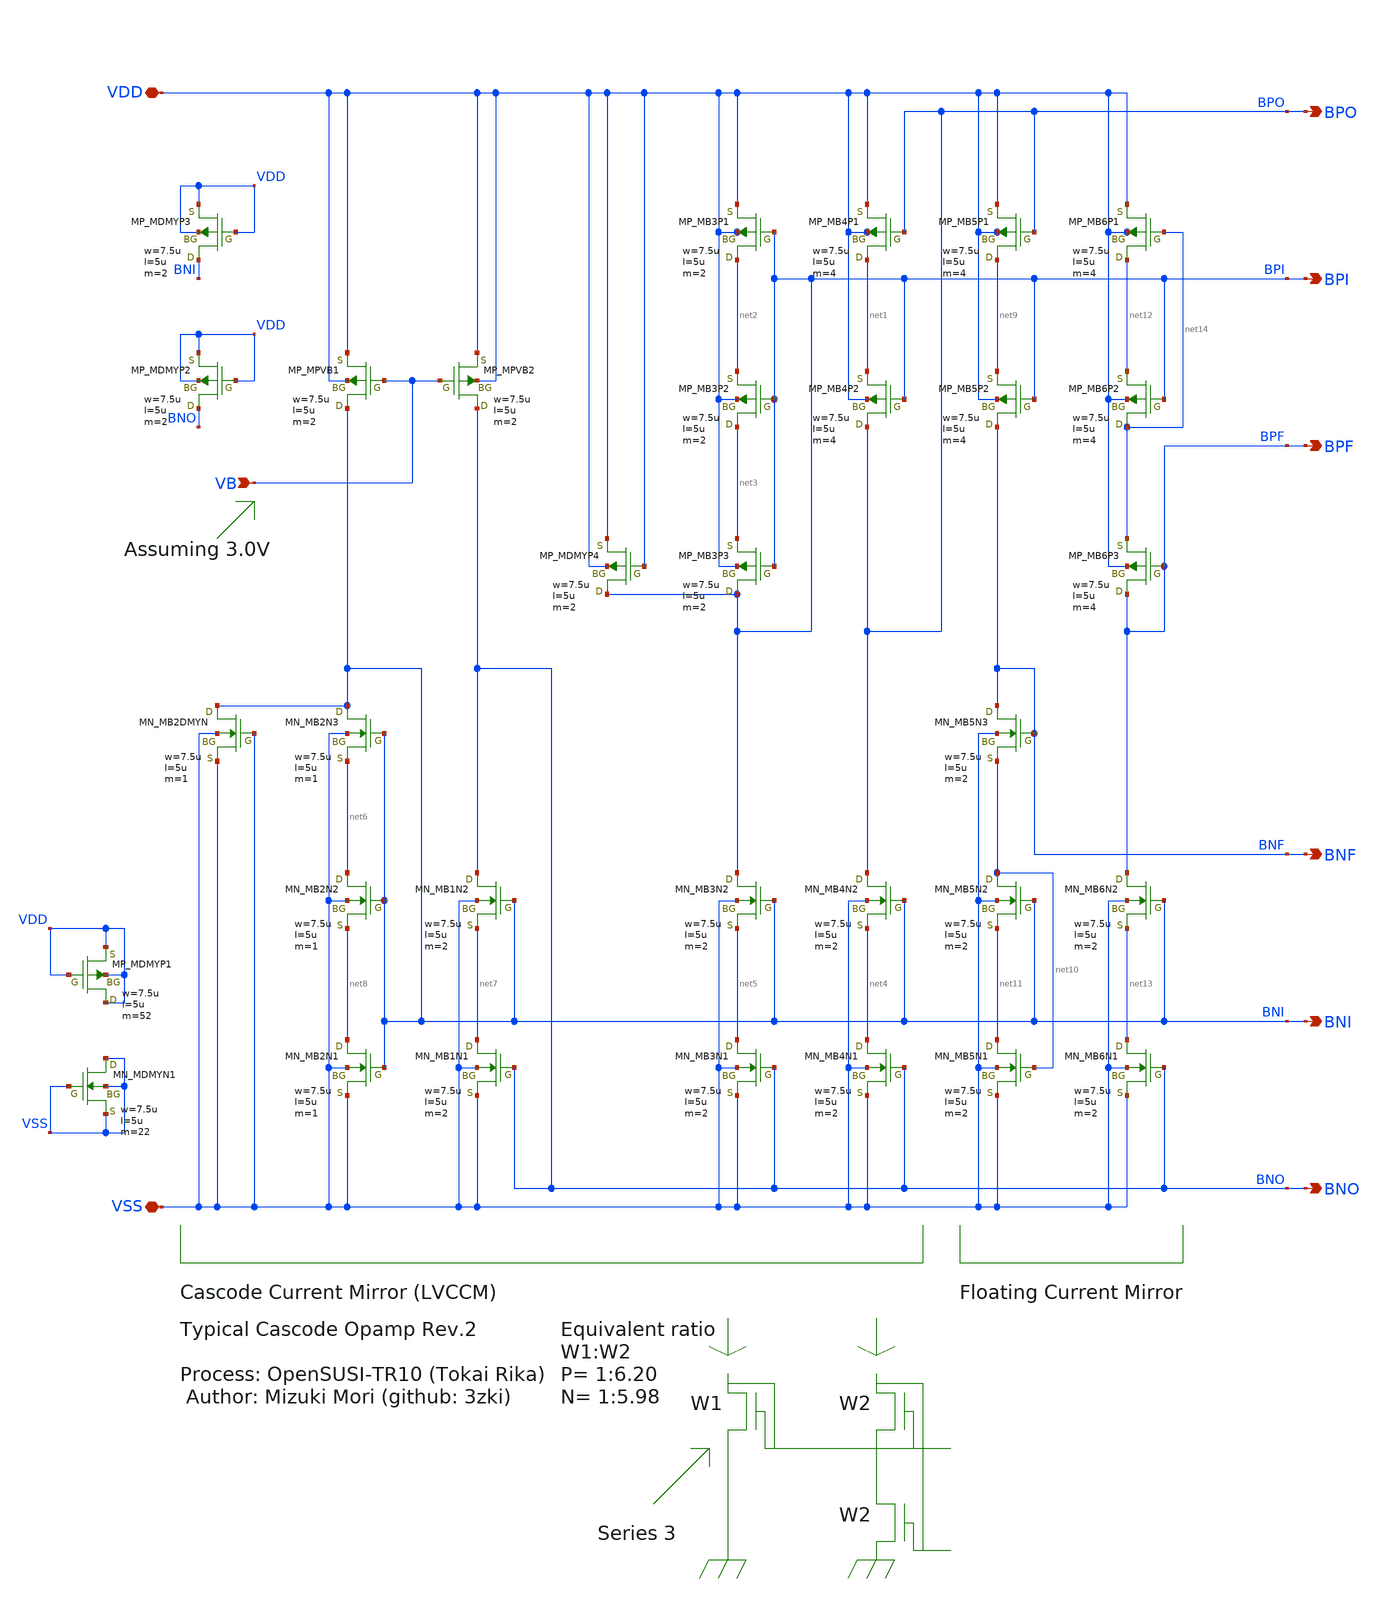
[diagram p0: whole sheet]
** sch_path: OpenSUSI-TR10/opamp_r2r_audio/opamp_r2r_CS.sch
**.subckt opamp_r2r_CS VDD VSS VB BPO BPI BPF BNF BNI BNO
*.iopin VDD
*.iopin VSS
*.ipin VB
*.opin BPO
*.opin BPI
*.opin BPF
*.opin BNF
*.opin BNI
*.opin BNO
XMB4P1 net1 BPO VDD VDD PMOS w=7.5u l=5u as=0 ad=0 ps=0 pd=0 nrd=0 nrs=0 m=4
XMB4P2 BPO BPI net1 VDD PMOS w=7.5u l=5u as=0 ad=0 ps=0 pd=0 nrd=0 nrs=0 m=4
XMB3P1 net2 BPI VDD VDD PMOS w=7.5u l=5u as=0 ad=0 ps=0 pd=0 nrd=0 nrs=0 m=2
XMB3P2 net3 BPI net2 VDD PMOS w=7.5u l=5u as=0 ad=0 ps=0 pd=0 nrd=0 nrs=0 m=2
XMB3P3 BPI BPI net3 VDD PMOS w=7.5u l=5u as=0 ad=0 ps=0 pd=0 nrd=0 nrs=0 m=2
XMB4N2 BPO BNI net4 VSS NMOS w=7.5u l=5u as=0 ad=0 ps=0 pd=0 nrd=0 nrs=0 m=2
XMB3N2 BPI BNI net5 VSS NMOS w=7.5u l=5u as=0 ad=0 ps=0 pd=0 nrd=0 nrs=0 m=2
XMB4N1 net4 BNO VSS VSS NMOS w=7.5u l=5u as=0 ad=0 ps=0 pd=0 nrd=0 nrs=0 m=2
XMB3N1 net5 BNO VSS VSS NMOS w=7.5u l=5u as=0 ad=0 ps=0 pd=0 nrd=0 nrs=0 m=2
XMB1N2 BNO BNI net7 VSS NMOS w=7.5u l=5u as=0 ad=0 ps=0 pd=0 nrd=0 nrs=0 m=2
XMB2N2 net6 BNI net8 VSS NMOS w=7.5u l=5u as=0 ad=0 ps=0 pd=0 nrd=0 nrs=0 m=1
XMB1N1 net7 BNO VSS VSS NMOS w=7.5u l=5u as=0 ad=0 ps=0 pd=0 nrd=0 nrs=0 m=2
XMB2N1 net8 BNI VSS VSS NMOS w=7.5u l=5u as=0 ad=0 ps=0 pd=0 nrd=0 nrs=0 m=1
XMB2N3 BNI BNI net6 VSS NMOS w=7.5u l=5u as=0 ad=0 ps=0 pd=0 nrd=0 nrs=0 m=1
XMB5P1 net9 BPO VDD VDD PMOS w=7.5u l=5u as=0 ad=0 ps=0 pd=0 nrd=0 nrs=0 m=4
XMB5P2 BNF BPI net9 VDD PMOS w=7.5u l=5u as=0 ad=0 ps=0 pd=0 nrd=0 nrs=0 m=4
XMB5N2 net10 BNI net11 VSS NMOS w=7.5u l=5u as=0 ad=0 ps=0 pd=0 nrd=0 nrs=0 m=2
XMB5N1 net11 net10 VSS VSS NMOS w=7.5u l=5u as=0 ad=0 ps=0 pd=0 nrd=0 nrs=0 m=2
XMB5N3 BNF BNF net10 VSS NMOS w=7.5u l=5u as=0 ad=0 ps=0 pd=0 nrd=0 nrs=0 m=2
XMB6P1 net12 net14 VDD VDD PMOS w=7.5u l=5u as=0 ad=0 ps=0 pd=0 nrd=0 nrs=0 m=4
XMB6P2 net14 BPI net12 VDD PMOS w=7.5u l=5u as=0 ad=0 ps=0 pd=0 nrd=0 nrs=0 m=4
XMB6N2 BPF BNI net13 VSS NMOS w=7.5u l=5u as=0 ad=0 ps=0 pd=0 nrd=0 nrs=0 m=2
XMB6N1 net13 BNO VSS VSS NMOS w=7.5u l=5u as=0 ad=0 ps=0 pd=0 nrd=0 nrs=0 m=2
XMB6P3 BPF BPF net14 VDD PMOS w=7.5u l=5u as=0 ad=0 ps=0 pd=0 nrd=0 nrs=0 m=4
XMB2DMYN BNI VSS VSS VSS NMOS w=7.5u l=5u as=0 ad=0 ps=0 pd=0 nrd=0 nrs=0 m=1
XMDMYN1 VSS VSS VSS VSS NMOS w=7.5u l=5u as=0 ad=0 ps=0 pd=0 nrd=0 nrs=0 m=22
XMDMYP1 VDD VDD VDD VDD PMOS w=7.5u l=5u as=0 ad=0 ps=0 pd=0 nrd=0 nrs=0 m=52
XMPVB1 BNI VB VDD VDD PMOS w=7.5u l=5u as=0 ad=0 ps=0 pd=0 nrd=0 nrs=0 m=2
XMPVB2 BNO VB VDD VDD PMOS w=7.5u l=5u as=0 ad=0 ps=0 pd=0 nrd=0 nrs=0 m=2
XMDMYP2 BNO VDD VDD VDD PMOS w=7.5u l=5u as=0 ad=0 ps=0 pd=0 nrd=0 nrs=0 m=2
XMDMYP3 BNI VDD VDD VDD PMOS w=7.5u l=5u as=0 ad=0 ps=0 pd=0 nrd=0 nrs=0 m=2
XMDMYP4 BPI VDD VDD VDD PMOS w=7.5u l=5u as=0 ad=0 ps=0 pd=0 nrd=0 nrs=0 m=2
**.ends
.end
